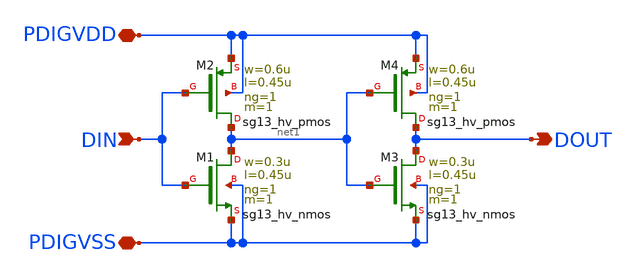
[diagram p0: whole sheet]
** sch_path: xschem/down_digital_translator.sch
**.subckt down_digital_translator PDIGVDD DIN DOUT PDIGVSS
*.iopin PDIGVDD
*.ipin DIN
*.opin DOUT
*.iopin PDIGVSS
XM1 net1 DIN PDIGVSS PDIGVSS sg13_hv_nmos w=0.3u l=0.45u ng=1 m=1 mm_ok=1
XM2 net1 DIN PDIGVDD PDIGVDD sg13_hv_pmos w=0.6u l=0.45u ng=1 m=1 mm_ok=1
XM3 DOUT net1 PDIGVSS PDIGVSS sg13_hv_nmos w=0.3u l=0.45u ng=1 m=1 mm_ok=1
XM4 DOUT net1 PDIGVDD PDIGVDD sg13_hv_pmos w=0.6u l=0.45u ng=1 m=1 mm_ok=1
**.ends
.end
